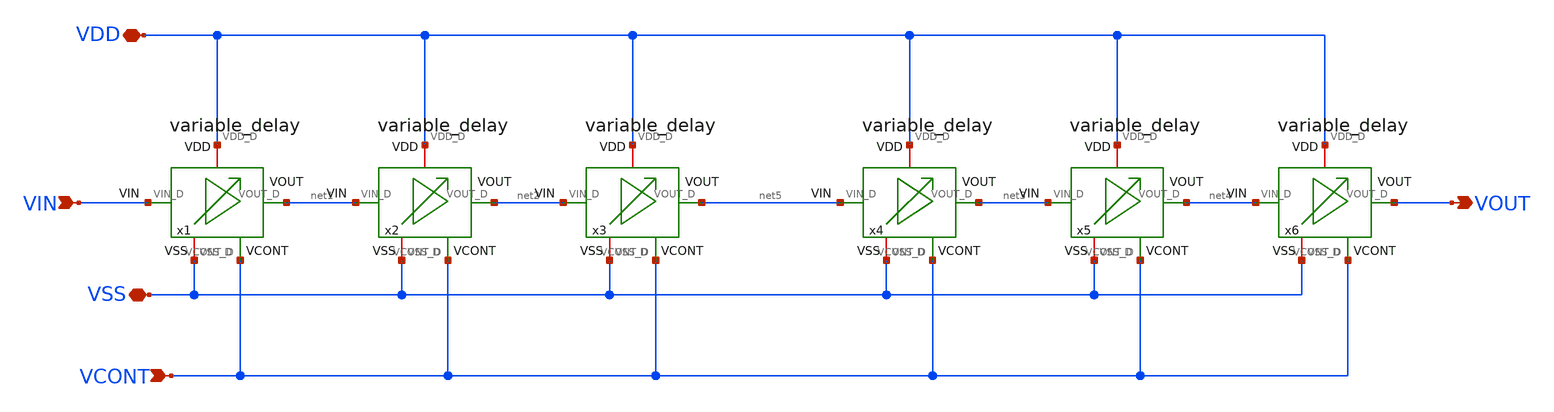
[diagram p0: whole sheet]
** sch_path: variable_delay_line.sch
**.subckt variable_delay_line VSS VDD VIN VOUT VCONT
*.iopin VSS
*.iopin VDD
*.ipin VIN
*.opin VOUT
*.ipin VCONT
x1 VDD VIN net1 VCONT VSS variable_delay
x2 VDD net1 net2 VCONT VSS variable_delay
x3 VDD net2 net5 VCONT VSS variable_delay
x4 VDD net5 net3 VCONT VSS variable_delay
x5 VDD net3 net4 VCONT VSS variable_delay
x6 VDD net4 VOUT VCONT VSS variable_delay
**.ends

* expanding   symbol:  /foss/designs/DLL/variable_delay.sym # of pins=5
** sym_path: variable_delay.sym
** sch_path: variable_delay.sch
.subckt variable_delay VDD_D VIN_D VOUT_D VCONT_D VSS_D
*.iopin VSS_D
*.iopin VDD_D
*.ipin VIN_D
*.opin VOUT_D
*.ipin VCONT_D
XM3 net4 VCONT_D net2 net2 sg13_lv_nmos w=1u l=0.13u ng=1 m=1 mm_ok=1
XM5 net3 VCONT_D net2 net2 sg13_lv_nmos w=1u l=5u ng=1 m=1 mm_ok=1
XM4 net4 net4 VDD_D VDD_D sg13_lv_pmos w=1u l=0.13u ng=1 m=1 mm_ok=1
XM6 net1 net4 VDD_D VDD_D sg13_lv_pmos w=1u l=5u ng=1 m=1 mm_ok=1
XM2 VOUT_D VIN_D net1 VDD_D sg13_lv_pmos w=10u l=10u ng=1 m=1 mm_ok=1
XM1 VOUT_D VIN_D net3 net2 sg13_lv_nmos w=10u l=10u ng=1 m=1 mm_ok=1
.ends

.end
